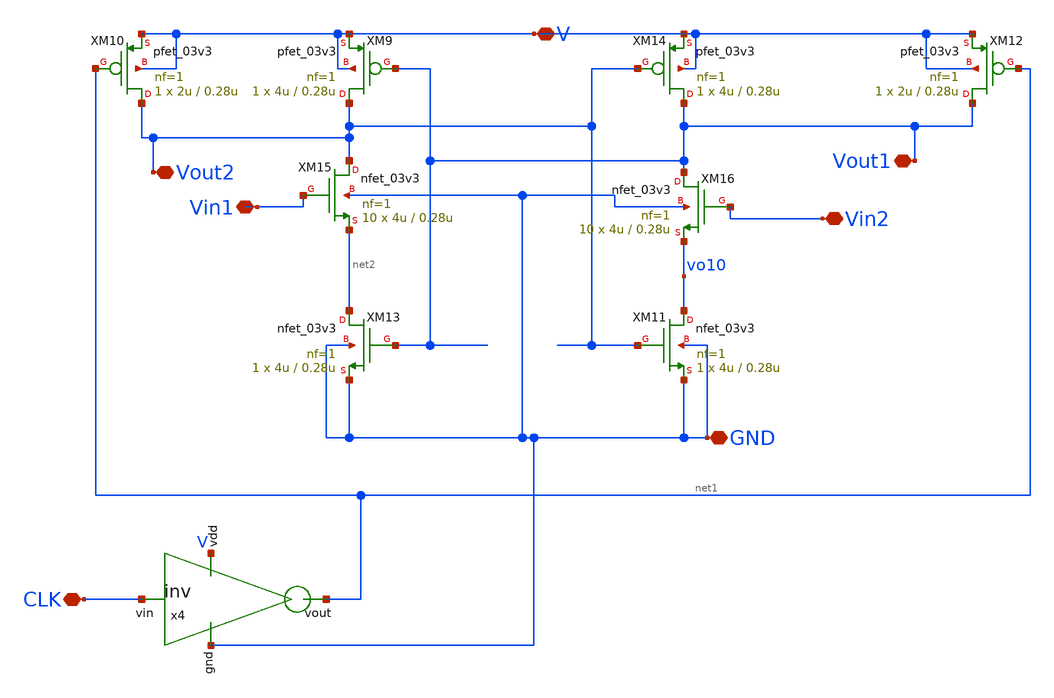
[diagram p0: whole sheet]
** sch_path: xschem/designs/strongarm.sch
**.subckt strongarm V Vout1 Vin1 Vin2 Vout2 CLK GND
*.iopin V
*.iopin Vout1
*.iopin Vin1
*.iopin Vin2
*.iopin Vout2
*.iopin CLK
*.iopin GND
XM9 Vout2 Vout1 V V pfet_03v3 L=0.28u W=4u nf=1 ad='int((nf+1)/2) * W/nf * 0.18u' as='int((nf+2)/2) * W/nf * 0.18u'
+ pd='2*int((nf+1)/2) * (W/nf + 0.18u)' ps='2*int((nf+2)/2) * (W/nf + 0.18u)' nrd='0.18u / W' nrs='0.18u / W'
+ sa=0 sb=0 sd=0 m=1
XM10 Vout2 net1 V V pfet_03v3 L=0.28u W=2u nf=1 ad='int((nf+1)/2) * W/nf * 0.18u' as='int((nf+2)/2) * W/nf * 0.18u'
+ pd='2*int((nf+1)/2) * (W/nf + 0.18u)' ps='2*int((nf+2)/2) * (W/nf + 0.18u)' nrd='0.18u / W' nrs='0.18u / W'
+ sa=0 sb=0 sd=0 m=1
XM11 vo10 Vout2 GND GND nfet_03v3 L=0.28u W=4u nf=1 ad='int((nf+1)/2) * W/nf * 0.18u' as='int((nf+2)/2) * W/nf * 0.18u'
+ pd='2*int((nf+1)/2) * (W/nf + 0.18u)' ps='2*int((nf+2)/2) * (W/nf + 0.18u)' nrd='0.18u / W' nrs='0.18u / W'
+ sa=0 sb=0 sd=0 m=1
XM12 Vout1 net1 V V pfet_03v3 L=0.28u W=2u nf=1 ad='int((nf+1)/2) * W/nf * 0.18u' as='int((nf+2)/2) * W/nf * 0.18u'
+ pd='2*int((nf+1)/2) * (W/nf + 0.18u)' ps='2*int((nf+2)/2) * (W/nf + 0.18u)' nrd='0.18u / W' nrs='0.18u / W'
+ sa=0 sb=0 sd=0 m=1
XM13 net2 Vout1 GND GND nfet_03v3 L=0.28u W=4u nf=1 ad='int((nf+1)/2) * W/nf * 0.18u' as='int((nf+2)/2) * W/nf * 0.18u'
+ pd='2*int((nf+1)/2) * (W/nf + 0.18u)' ps='2*int((nf+2)/2) * (W/nf + 0.18u)' nrd='0.18u / W' nrs='0.18u / W'
+ sa=0 sb=0 sd=0 m=1
XM14 Vout1 Vout2 V V pfet_03v3 L=0.28u W=4u nf=1 ad='int((nf+1)/2) * W/nf * 0.18u' as='int((nf+2)/2) * W/nf * 0.18u'
+ pd='2*int((nf+1)/2) * (W/nf + 0.18u)' ps='2*int((nf+2)/2) * (W/nf + 0.18u)' nrd='0.18u / W' nrs='0.18u / W'
+ sa=0 sb=0 sd=0 m=1
XM15 Vout2 Vin1 net2 GND nfet_03v3 L=0.28u W=4u nf=1 ad='int((nf+1)/2) * W/nf * 0.18u' as='int((nf+2)/2) * W/nf * 0.18u'
+ pd='2*int((nf+1)/2) * (W/nf + 0.18u)' ps='2*int((nf+2)/2) * (W/nf + 0.18u)' nrd='0.18u / W' nrs='0.18u / W'
+ sa=0 sb=0 sd=0 m=10
XM16 Vout1 Vin2 vo10 GND nfet_03v3 L=0.28u W=4u nf=1 ad='int((nf+1)/2) * W/nf * 0.18u' as='int((nf+2)/2) * W/nf * 0.18u'
+ pd='2*int((nf+1)/2) * (W/nf + 0.18u)' ps='2*int((nf+2)/2) * (W/nf + 0.18u)' nrd='0.18u / W' nrs='0.18u / W'
+ sa=0 sb=0 sd=0 m=10
x4 V GND net1 CLK inv cl=0.28u wp=0.44u wn=0.22u wx=5u mx=1
**.ends

* expanding   symbol:  inv.sym # of pins=4
** sym_path: xschem/designs/inv.sym
** sch_path: xschem/designs/inv.sch
.subckt inv vdd gnd vout vin  cl=0.28u wp=0.44u wn=0.22u wx=0.22u mx=1
*.ipin gnd
*.ipin vdd
*.ipin vin
*.opin vout
XM1 gnd vin vout gnd nfet_03v3 L=0.28u W=Wx nf=1 ad='int((nf+1)/2) * W/nf * 0.18u' as='int((nf+2)/2) * W/nf * 0.18u'
+ pd='2*int((nf+1)/2) * (W/nf + 0.18u)' ps='2*int((nf+2)/2) * (W/nf + 0.18u)' nrd='0.18u / W' nrs='0.18u / W'
+ sa=0 sb=0 sd=0 m=1
XM2 vdd vin vout vdd pfet_03v3 L=0.28u W=Wx nf=1 ad='int((nf+1)/2) * W/nf * 0.18u' as='int((nf+2)/2) * W/nf * 0.18u'
+ pd='2*int((nf+1)/2) * (W/nf + 0.18u)' ps='2*int((nf+2)/2) * (W/nf + 0.18u)' nrd='0.18u / W' nrs='0.18u / W'
+ sa=0 sb=0 sd=0 m=1
.ends

.end
